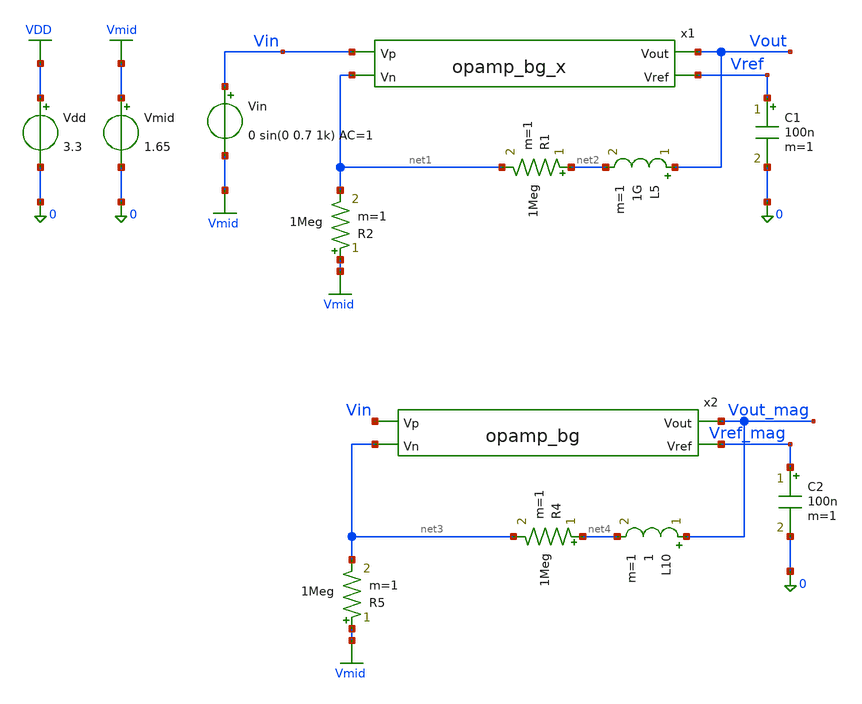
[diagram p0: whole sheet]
** sch_path: xschem/opamp_x_tb.sch
* Copyright 2021 Stefan Frederik Schippers
* Licensed under the Apache License, Version 2.0 (the "License");
* you may not use this file except in compliance with the License.
* You may obtain a copy of the License at
* https://www.apache.org/licenses/LICENSE-2.0
* Unless required by applicable law or agreed to in writing, software
* distributed under the License is distributed on an "AS IS" BASIS,
* WITHOUT WARRANTIES OR CONDITIONS OF ANY KIND, either express or implied.
* See the License for the specific language governing permissions and
* limitations under the License.
**.subckt opamp_x_tb
Vdd VDD 0 3.3
C1 Vref 0 100n m=1
Vin Vin Vmid 0 sin(0 0.7 1k) AC=1
R1 net2 net1 1Meg m=1
R2 Vmid net1 1Meg m=1
Vmid Vmid 0 1.65
L5 Vout net2 1G m=1
x2 Vin Vout_mag net3 Vref_mag opamp_bg
x1 Vin Vout net1 Vref opamp_bg_x
C2 Vref_mag 0 100n m=1
R4 net4 net3 1Meg m=1
R5 Vmid net3 1Meg m=1
L10 Vout_mag net4 1 m=1
**** begin user architecture code

** opencircuitdesign pdks install
.lib $::SKYWATER_MODELS/sky130.lib.spice tt



.option wnflag=1
.option savecurrents
.option rshunt=1e12
.include ../gds/opamp.spice
.save all
.control
op
write opamp_x_tb.raw
print Vref I(v.x1.x2.vmeas_iref) V(x1.x2.Vg1)
if 0
alter L5 1n
tran 1u 2m
plot V(Vin) V(Vout) title 'Vin and Vout vs time'
endif

alter L5 10G
alter L10 10G
ac dec 100 1 100Meg
plot db(V(Vout)) db(V(Vout_mag)) title 'Vout vs Vout_mag Open loop'
*plot cph(V(vout))*180/pi title 'Phase Vout open loop'

if 1
alter L5 1n
alter L10 1n
alter R1 1m
alter R4 1m
ac dec 100 1 100Meg
plot db(V(Vout)) db(V(Vout_mag)) title 'Mag Unity gain'
*plot cph(V(vout))*180/pi title 'Phase Vout Unity gain'
endif

.endc


**** end user architecture code
**.ends
.GLOBAL VDD
.GLOBAL Vmid
.end
